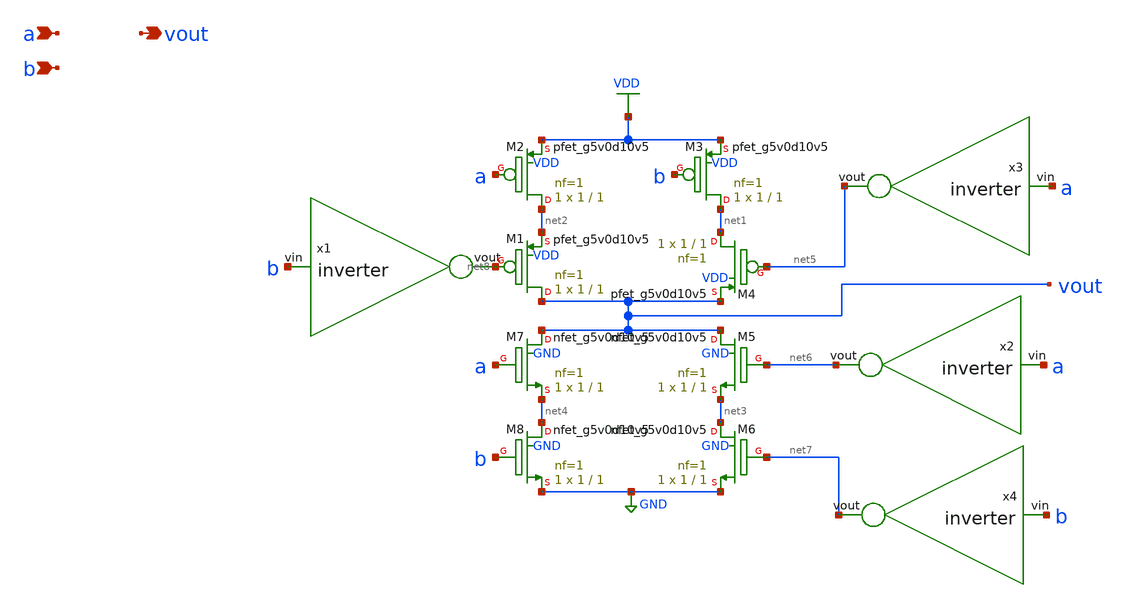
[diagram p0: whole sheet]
** sch_path: schematics/xor.sch
**.subckt xor a b vout
*.ipin a
*.ipin b
*.opin vout
XM2 net2 a VDD VDD sky130_fd_pr__pfet_g5v0d10v5 L=1 W=1 nf=1 ad='int((nf+1)/2) * W/nf * 0.29' as='int((nf+2)/2) * W/nf * 0.29'
+ pd='2*int((nf+1)/2) * (W/nf + 0.29)' ps='2*int((nf+2)/2) * (W/nf + 0.29)' nrd='0.29 / W' nrs='0.29 / W'
+ sa=0 sb=0 sd=0 mult=1 m=1
XM3 net1 b VDD VDD sky130_fd_pr__pfet_g5v0d10v5 L=1 W=1 nf=1 ad='int((nf+1)/2) * W/nf * 0.29' as='int((nf+2)/2) * W/nf * 0.29'
+ pd='2*int((nf+1)/2) * (W/nf + 0.29)' ps='2*int((nf+2)/2) * (W/nf + 0.29)' nrd='0.29 / W' nrs='0.29 / W'
+ sa=0 sb=0 sd=0 mult=1 m=1
XM8 net4 b GND GND sky130_fd_pr__nfet_g5v0d10v5 L=1 W=1 nf=1 ad='int((nf+1)/2) * W/nf * 0.29' as='int((nf+2)/2) * W/nf * 0.29'
+ pd='2*int((nf+1)/2) * (W/nf + 0.29)' ps='2*int((nf+2)/2) * (W/nf + 0.29)' nrd='0.29 / W' nrs='0.29 / W'
+ sa=0 sb=0 sd=0 mult=1 m=1
XM7 vout a net4 GND sky130_fd_pr__nfet_g5v0d10v5 L=1 W=1 nf=1 ad='int((nf+1)/2) * W/nf * 0.29' as='int((nf+2)/2) * W/nf * 0.29'
+ pd='2*int((nf+1)/2) * (W/nf + 0.29)' ps='2*int((nf+2)/2) * (W/nf + 0.29)' nrd='0.29 / W' nrs='0.29 / W'
+ sa=0 sb=0 sd=0 mult=1 m=1
x1 net8 b inverter
XM1 vout net8 net2 VDD sky130_fd_pr__pfet_g5v0d10v5 L=1 W=1 nf=1 ad='int((nf+1)/2) * W/nf * 0.29' as='int((nf+2)/2) * W/nf * 0.29'
+ pd='2*int((nf+1)/2) * (W/nf + 0.29)' ps='2*int((nf+2)/2) * (W/nf + 0.29)' nrd='0.29 / W' nrs='0.29 / W'
+ sa=0 sb=0 sd=0 mult=1 m=1
x3 net5 a inverter
XM4 net1 net5 vout VDD sky130_fd_pr__pfet_g5v0d10v5 L=1 W=1 nf=1 ad='int((nf+1)/2) * W/nf * 0.29' as='int((nf+2)/2) * W/nf * 0.29'
+ pd='2*int((nf+1)/2) * (W/nf + 0.29)' ps='2*int((nf+2)/2) * (W/nf + 0.29)' nrd='0.29 / W' nrs='0.29 / W'
+ sa=0 sb=0 sd=0 mult=1 m=1
XM5 vout net6 net3 GND sky130_fd_pr__nfet_g5v0d10v5 L=1 W=1 nf=1 ad='int((nf+1)/2) * W/nf * 0.29' as='int((nf+2)/2) * W/nf * 0.29'
+ pd='2*int((nf+1)/2) * (W/nf + 0.29)' ps='2*int((nf+2)/2) * (W/nf + 0.29)' nrd='0.29 / W' nrs='0.29 / W'
+ sa=0 sb=0 sd=0 mult=1 m=1
XM6 net3 net7 GND GND sky130_fd_pr__nfet_g5v0d10v5 L=1 W=1 nf=1 ad='int((nf+1)/2) * W/nf * 0.29' as='int((nf+2)/2) * W/nf * 0.29'
+ pd='2*int((nf+1)/2) * (W/nf + 0.29)' ps='2*int((nf+2)/2) * (W/nf + 0.29)' nrd='0.29 / W' nrs='0.29 / W'
+ sa=0 sb=0 sd=0 mult=1 m=1
x2 net6 a inverter
x4 net7 b inverter
**.ends

* expanding   symbol:  /media/sf_share/final_project/inverter.sym # of pins=2
** sym_path: schematics/inverter.sym
** sch_path: schematics/inverter.sch
.subckt inverter vout vin
*.ipin vin
*.opin vout
XM3 vout vin VDD VDD sky130_fd_pr__pfet_g5v0d10v5 L=0.5 W=0.5 nf=1 ad='int((nf+1)/2) * W/nf * 0.29' as='int((nf+2)/2) * W/nf * 0.29'
+ pd='2*int((nf+1)/2) * (W/nf + 0.29)' ps='2*int((nf+2)/2) * (W/nf + 0.29)' nrd='0.29 / W' nrs='0.29 / W'
+ sa=0 sb=0 sd=0 mult=1 m=1
XM5 vout vin GND GND sky130_fd_pr__nfet_g5v0d10v5 L=0.5 W=0.5 nf=1 ad='int((nf+1)/2) * W/nf * 0.29' as='int((nf+2)/2) * W/nf * 0.29'
+ pd='2*int((nf+1)/2) * (W/nf + 0.29)' ps='2*int((nf+2)/2) * (W/nf + 0.29)' nrd='0.29 / W' nrs='0.29 / W'
+ sa=0 sb=0 sd=0 mult=1 m=1
.ends

.GLOBAL VDD
.GLOBAL GND
.end
